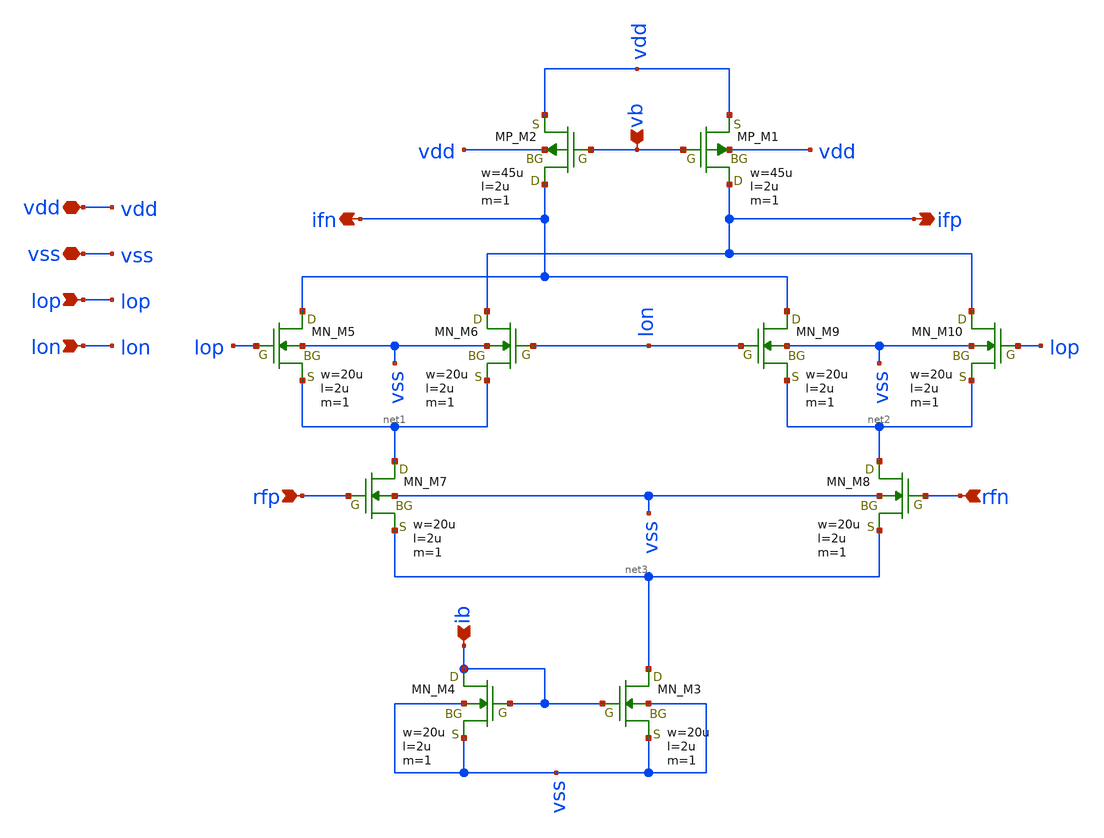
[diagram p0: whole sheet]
** sch_path: member_project/JJY_Receiver/Masahiro/jjy_recv/gilbert_cell/gilbert_cell.sch
**.subckt gilbert_cell ifp ifn rfp vb ib rfn vdd vss lon lop
*.opin ifp
*.opin ifn
*.ipin rfp
*.ipin vb
*.ipin ib
*.ipin rfn
*.iopin vdd
*.iopin vss
*.ipin lon
*.ipin lop
XM1 ifp vb vdd vdd PMOS w=45u l=2u as=0 ad=0 ps=0 pd=0 nrd=0 nrs=0 m=1
XM2 ifn vb vdd vdd PMOS w=45u l=2u as=0 ad=0 ps=0 pd=0 nrd=0 nrs=0 m=1
XM3 net3 ib vss vss NMOS w=20u l=2u as=0 ad=0 ps=0 pd=0 nrd=0 nrs=0 m=1
XM4 ib ib vss vss NMOS w=20u l=2u as=0 ad=0 ps=0 pd=0 nrd=0 nrs=0 m=1
XM7 net1 rfp net3 vss NMOS w=20u l=2u as=0 ad=0 ps=0 pd=0 nrd=0 nrs=0 m=1
XM8 net2 rfn net3 vss NMOS w=20u l=2u as=0 ad=0 ps=0 pd=0 nrd=0 nrs=0 m=1
XM5 ifn lop net1 vss NMOS w=20u l=2u as=0 ad=0 ps=0 pd=0 nrd=0 nrs=0 m=1
XM6 ifp lon net1 vss NMOS w=20u l=2u as=0 ad=0 ps=0 pd=0 nrd=0 nrs=0 m=1
XM9 ifn lon net2 vss NMOS w=20u l=2u as=0 ad=0 ps=0 pd=0 nrd=0 nrs=0 m=1
XM10 ifp lop net2 vss NMOS w=20u l=2u as=0 ad=0 ps=0 pd=0 nrd=0 nrs=0 m=1
**** begin user architecture code
 .include $::LIB/ip62_models
**** end user architecture code
**.ends
.end
